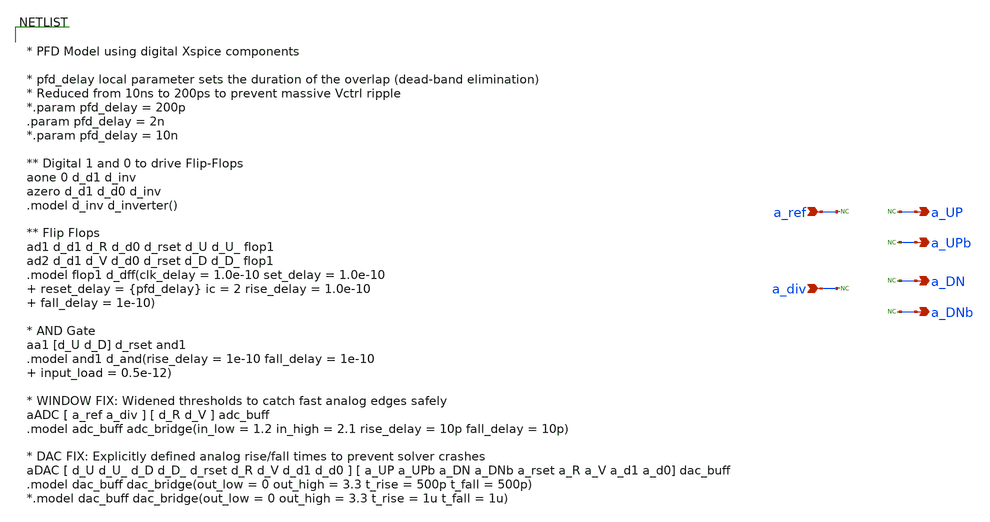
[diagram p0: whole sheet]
** sch_path: designs/libs/model_pll/pfd_model.sch
**.subckt pfd_model a_ref a_div a_UP a_UPb a_DN a_DNb
*.ipin a_ref
*.ipin a_div
*.opin a_UP
*.opin a_UPb
*.opin a_DN
*.opin a_DNb
* noconn a_ref
* noconn a_div
* noconn a_UP
* noconn a_UPb
* noconn a_DN
* noconn a_DNb
**** begin user architecture code


* PFD Model using digital Xspice components

* pfd_delay local parameter sets the duration of the overlap (dead-band elimination)
* Reduced from 10ns to 200ps to prevent massive Vctrl ripple
*.param pfd_delay = 200p
.param pfd_delay = 2n
*.param pfd_delay = 10n

** Digital 1 and 0 to drive Flip-Flops
aone 0 d_d1 d_inv
azero d_d1 d_d0 d_inv
.model d_inv d_inverter()

** Flip Flops
ad1 d_d1 d_R d_d0 d_rset d_U d_U_ flop1
ad2 d_d1 d_V d_d0 d_rset d_D d_D_ flop1
.model flop1 d_dff(clk_delay = 1.0e-10 set_delay = 1.0e-10  reset_delay = {pfd_delay} ic = 2 rise_delay
+ = 1.0e-10  fall_delay = 1e-10)

* AND Gate
aa1 [d_U d_D] d_rset and1
.model and1 d_and(rise_delay = 1e-10 fall_delay = 1e-10   input_load = 0.5e-12)

* WINDOW FIX: Widened thresholds to catch fast analog edges safely
aADC [ a_ref a_div ] [ d_R d_V ] adc_buff
.model adc_buff adc_bridge(in_low = 1.2 in_high = 2.1 rise_delay = 10p fall_delay = 10p)

* DAC FIX: Explicitly defined analog rise/fall times to prevent solver crashes
aDAC [ d_U d_U_ d_D d_D_ d_rset d_R d_V d_d1 d_d0 ] [ a_UP a_UPb a_DN a_DNb a_rset a_R a_V a_d1
+ a_d0] dac_buff
.model dac_buff dac_bridge(out_low = 0 out_high = 3.3 t_rise = 500p t_fall = 500p)
*.model dac_buff dac_bridge(out_low = 0 out_high = 3.3 t_rise = 1u t_fall = 1u)


**** end user architecture code
**.ends
.end
